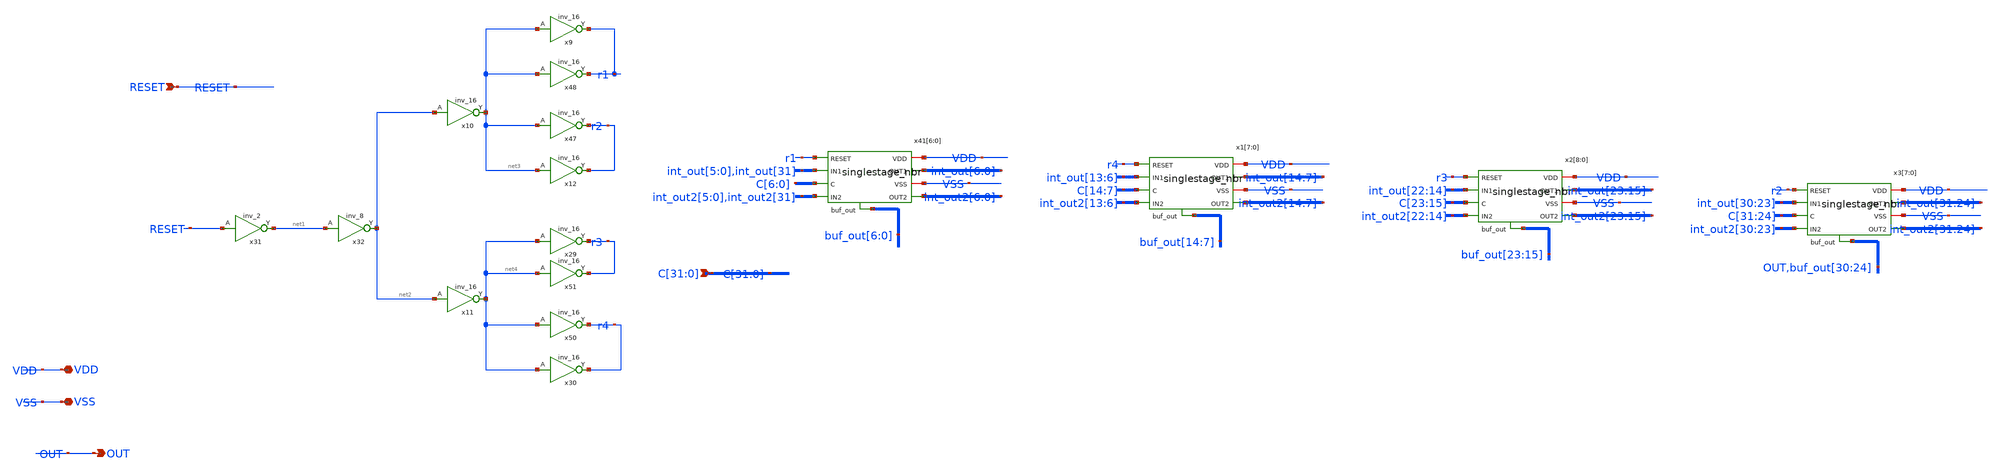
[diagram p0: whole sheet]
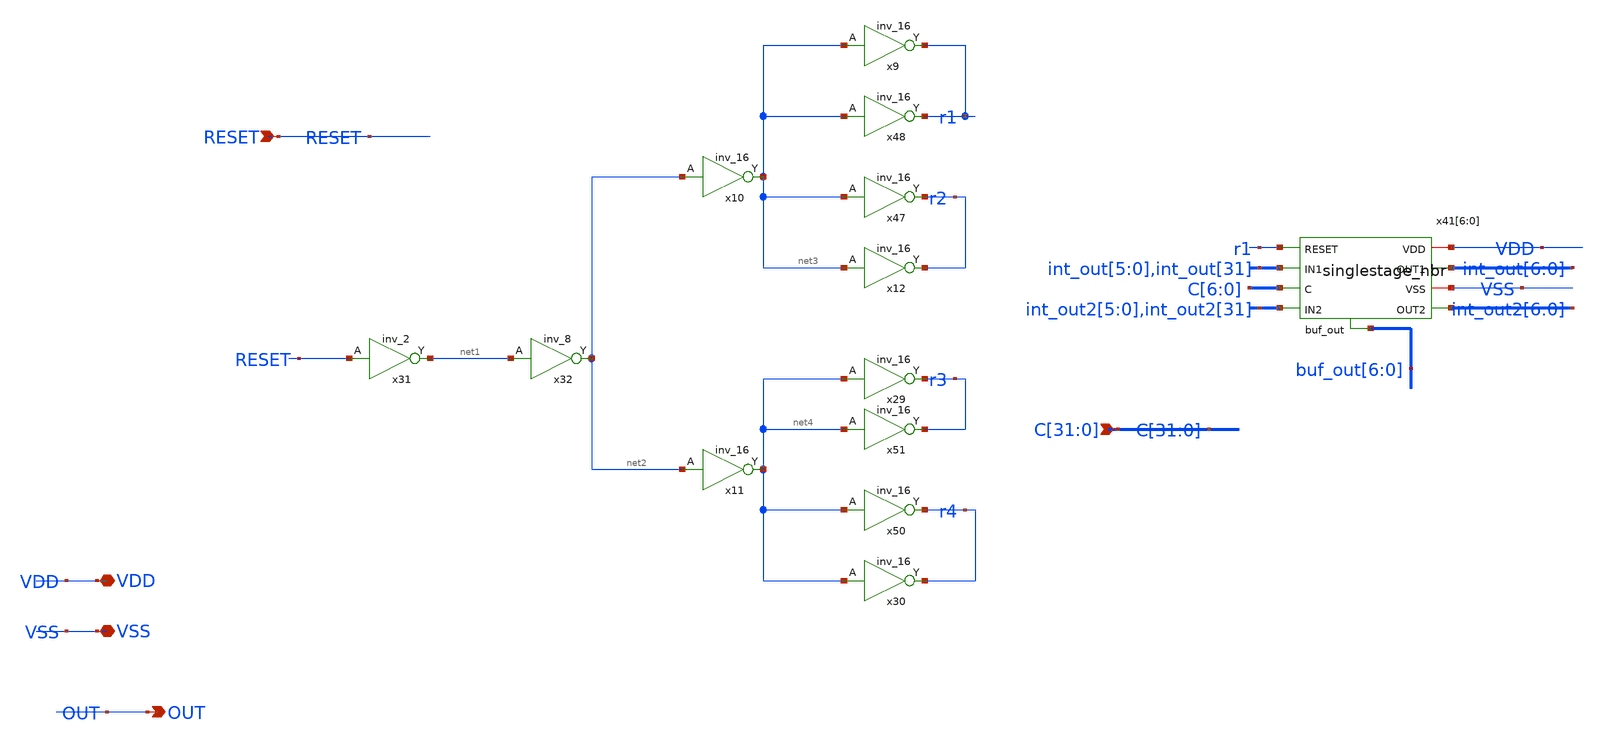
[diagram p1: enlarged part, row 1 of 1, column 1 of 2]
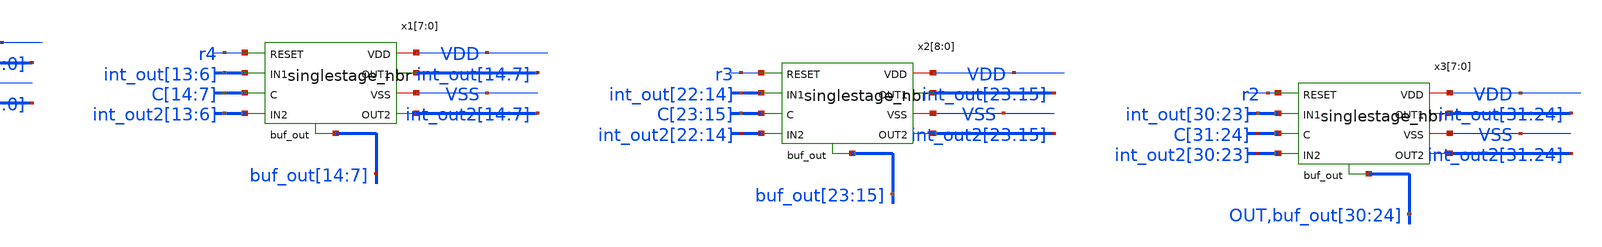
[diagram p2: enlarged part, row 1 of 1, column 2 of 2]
** sch_path: design/NBR32.sch
**.subckt NBR32 VDD VSS RESET OUT
*+ C[31],C[30],C[29],C[28],C[27],C[26],C[25],C[24],C[23],C[22],C[21],C[20],C[19],C[18],C[17],C[16],C[15],C[14],C[13],C[12],C[11],C[10],C[9],C[8],C[7],C[6],C[5],C[4],C[3],C[2],C[1],C[0]
*.iopin VDD
*.iopin VSS
*.ipin RESET
*.opin OUT
*.ipin
*+ C[31],C[30],C[29],C[28],C[27],C[26],C[25],C[24],C[23],C[22],C[21],C[20],C[19],C[18],C[17],C[16],C[15],C[14],C[13],C[12],C[11],C[10],C[9],C[8],C[7],C[6],C[5],C[4],C[3],C[2],C[1],C[0]
x47 net3 VSS VSS VDD VDD r2 sky130_fd_sc_hd__inv_16
x48 net3 VSS VSS VDD VDD r1 sky130_fd_sc_hd__inv_16
x50 net4 VSS VSS VDD VDD r4 sky130_fd_sc_hd__inv_16
x51 net4 VSS VSS VDD VDD r3 sky130_fd_sc_hd__inv_16
x9 net3 VSS VSS VDD VDD r1 sky130_fd_sc_hd__inv_16
x10 net2 VSS VSS VDD VDD net3 sky130_fd_sc_hd__inv_16
x11 net2 VSS VSS VDD VDD net4 sky130_fd_sc_hd__inv_16
x12 net3 VSS VSS VDD VDD r2 sky130_fd_sc_hd__inv_16
x29 net4 VSS VSS VDD VDD r3 sky130_fd_sc_hd__inv_16
x30 net4 VSS VSS VDD VDD r4 sky130_fd_sc_hd__inv_16
x31 RESET VSS VSS VDD VDD net1 sky130_fd_sc_hd__inv_2
x32 net1 VSS VSS VDD VDD net2 sky130_fd_sc_hd__inv_8
x41[6] r1 VDD VSS int_out[6] int_out[5] buf_out[6] C[6] int_out2[5] int_out2[6] singlestage_nbr
x41[5] r1 VDD VSS int_out[5] int_out[4] buf_out[5] C[5] int_out2[4] int_out2[5] singlestage_nbr
x41[4] r1 VDD VSS int_out[4] int_out[3] buf_out[4] C[4] int_out2[3] int_out2[4] singlestage_nbr
x41[3] r1 VDD VSS int_out[3] int_out[2] buf_out[3] C[3] int_out2[2] int_out2[3] singlestage_nbr
x41[2] r1 VDD VSS int_out[2] int_out[1] buf_out[2] C[2] int_out2[1] int_out2[2] singlestage_nbr
x41[1] r1 VDD VSS int_out[1] int_out[0] buf_out[1] C[1] int_out2[0] int_out2[1] singlestage_nbr
x41[0] r1 VDD VSS int_out[0] int_out[31] buf_out[0] C[0] int_out2[31] int_out2[0] singlestage_nbr
x1[7] r4 VDD VSS int_out[14] int_out[13] buf_out[14] C[14] int_out2[13] int_out2[14] singlestage_nbr
x1[6] r4 VDD VSS int_out[13] int_out[12] buf_out[13] C[13] int_out2[12] int_out2[13] singlestage_nbr
x1[5] r4 VDD VSS int_out[12] int_out[11] buf_out[12] C[12] int_out2[11] int_out2[12] singlestage_nbr
x1[4] r4 VDD VSS int_out[11] int_out[10] buf_out[11] C[11] int_out2[10] int_out2[11] singlestage_nbr
x1[3] r4 VDD VSS int_out[10] int_out[9] buf_out[10] C[10] int_out2[9] int_out2[10] singlestage_nbr
x1[2] r4 VDD VSS int_out[9] int_out[8] buf_out[9] C[9] int_out2[8] int_out2[9] singlestage_nbr
x1[1] r4 VDD VSS int_out[8] int_out[7] buf_out[8] C[8] int_out2[7] int_out2[8] singlestage_nbr
x1[0] r4 VDD VSS int_out[7] int_out[6] buf_out[7] C[7] int_out2[6] int_out2[7] singlestage_nbr
x2[8] r3 VDD VSS int_out[23] int_out[22] buf_out[23] C[23] int_out2[22] int_out2[23] singlestage_nbr
x2[7] r3 VDD VSS int_out[22] int_out[21] buf_out[22] C[22] int_out2[21] int_out2[22] singlestage_nbr
x2[6] r3 VDD VSS int_out[21] int_out[20] buf_out[21] C[21] int_out2[20] int_out2[21] singlestage_nbr
x2[5] r3 VDD VSS int_out[20] int_out[19] buf_out[20] C[20] int_out2[19] int_out2[20] singlestage_nbr
x2[4] r3 VDD VSS int_out[19] int_out[18] buf_out[19] C[19] int_out2[18] int_out2[19] singlestage_nbr
x2[3] r3 VDD VSS int_out[18] int_out[17] buf_out[18] C[18] int_out2[17] int_out2[18] singlestage_nbr
x2[2] r3 VDD VSS int_out[17] int_out[16] buf_out[17] C[17] int_out2[16] int_out2[17] singlestage_nbr
x2[1] r3 VDD VSS int_out[16] int_out[15] buf_out[16] C[16] int_out2[15] int_out2[16] singlestage_nbr
x2[0] r3 VDD VSS int_out[15] int_out[14] buf_out[15] C[15] int_out2[14] int_out2[15] singlestage_nbr
x3[7] r2 VDD VSS int_out[31] int_out[30] OUT C[31] int_out2[30] int_out2[31] singlestage_nbr
x3[6] r2 VDD VSS int_out[30] int_out[29] buf_out[30] C[30] int_out2[29] int_out2[30] singlestage_nbr
x3[5] r2 VDD VSS int_out[29] int_out[28] buf_out[29] C[29] int_out2[28] int_out2[29] singlestage_nbr
x3[4] r2 VDD VSS int_out[28] int_out[27] buf_out[28] C[28] int_out2[27] int_out2[28] singlestage_nbr
x3[3] r2 VDD VSS int_out[27] int_out[26] buf_out[27] C[27] int_out2[26] int_out2[27] singlestage_nbr
x3[2] r2 VDD VSS int_out[26] int_out[25] buf_out[26] C[26] int_out2[25] int_out2[26] singlestage_nbr
x3[1] r2 VDD VSS int_out[25] int_out[24] buf_out[25] C[25] int_out2[24] int_out2[25] singlestage_nbr
x3[0] r2 VDD VSS int_out[24] int_out[23] buf_out[24] C[24] int_out2[23] int_out2[24] singlestage_nbr
**.ends

* expanding   symbol:  singlestage_nbr.sym # of pins=9
** sym_path: design/singlestage_nbr.sym
** sch_path: design/singlestage_nbr.sch
.subckt singlestage_nbr RESET VDD VSS OUT1 IN1 buf_out C IN2 OUT2
*.ipin IN1
*.ipin C
*.ipin RESET
*.iopin VSS
*.iopin VDD
*.opin OUT2
*.opin buf_out
*.opin OUT1
*.ipin IN2
x1 RESET IN1 VSS VSS VDD VDD net1 sky130_fd_sc_hd__nor2_1
x2 RESET IN2 VSS VSS VDD VDD net2 sky130_fd_sc_hd__nor2_1
x5 Cb VSS VSS VDD VDD Cbb sky130_fd_sc_hd__inv_1
x6 C VSS VSS VDD VDD Cb sky130_fd_sc_hd__inv_1
x7 OUT2 VSS VSS VDD VDD net3 sky130_fd_sc_hd__buf_1
x3 Cbb VSS net1 VDD OUT2 Cb net2 mux2-1
x4 Cbb VSS net2 VDD OUT1 Cb net1 mux2-1
x8 OUT1 VSS VSS VDD VDD buf_out sky130_fd_sc_hd__buf_1
* noconn #net3
.ends


* expanding   symbol:  mux2-1.sym # of pins=7
** sym_path: design/mux2-1.sym
** sch_path: design/mux2-1.sch
.subckt mux2-1 S VSS IN1 VDD OUT Sbar IN2
*.ipin IN1
*.ipin IN2
*.ipin Sbar
*.ipin S
*.opin OUT
*.iopin VSS
*.iopin VDD
XM2 IN1 S OUT VSS sky130_fd_pr__nfet_01v8 L=0.15 W=0.65 nf=1 ad='int((nf+1)/2) * W/nf * 0.29' as='int((nf+2)/2) * W/nf * 0.29'
+ pd='2*int((nf+1)/2) * (W/nf + 0.29)' ps='2*int((nf+2)/2) * (W/nf + 0.29)' nrd='0.29 / W' nrs='0.29 / W'
+ sa=0 sb=0 sd=0 mult=1 m=1
XM1 IN2 Sbar OUT VSS sky130_fd_pr__nfet_01v8 L=0.15 W=0.65 nf=1 ad='int((nf+1)/2) * W/nf * 0.29' as='int((nf+2)/2) * W/nf * 0.29'
+ pd='2*int((nf+1)/2) * (W/nf + 0.29)' ps='2*int((nf+2)/2) * (W/nf + 0.29)' nrd='0.29 / W' nrs='0.29 / W'
+ sa=0 sb=0 sd=0 mult=1 m=1
XM4 IN1 Sbar OUT VDD sky130_fd_pr__pfet_01v8_hvt L=0.15 W=1 nf=1 ad='int((nf+1)/2) * W/nf * 0.29' as='int((nf+2)/2) * W/nf * 0.29'
+ pd='2*int((nf+1)/2) * (W/nf + 0.29)' ps='2*int((nf+2)/2) * (W/nf + 0.29)' nrd='0.29 / W' nrs='0.29 / W'
+ sa=0 sb=0 sd=0 mult=1 m=1
XM5 IN2 S OUT VDD sky130_fd_pr__pfet_01v8_hvt L=0.15 W=1 nf=1 ad='int((nf+1)/2) * W/nf * 0.29' as='int((nf+2)/2) * W/nf * 0.29'
+ pd='2*int((nf+1)/2) * (W/nf + 0.29)' ps='2*int((nf+2)/2) * (W/nf + 0.29)' nrd='0.29 / W' nrs='0.29 / W'
+ sa=0 sb=0 sd=0 mult=1 m=1
.ends

.end
